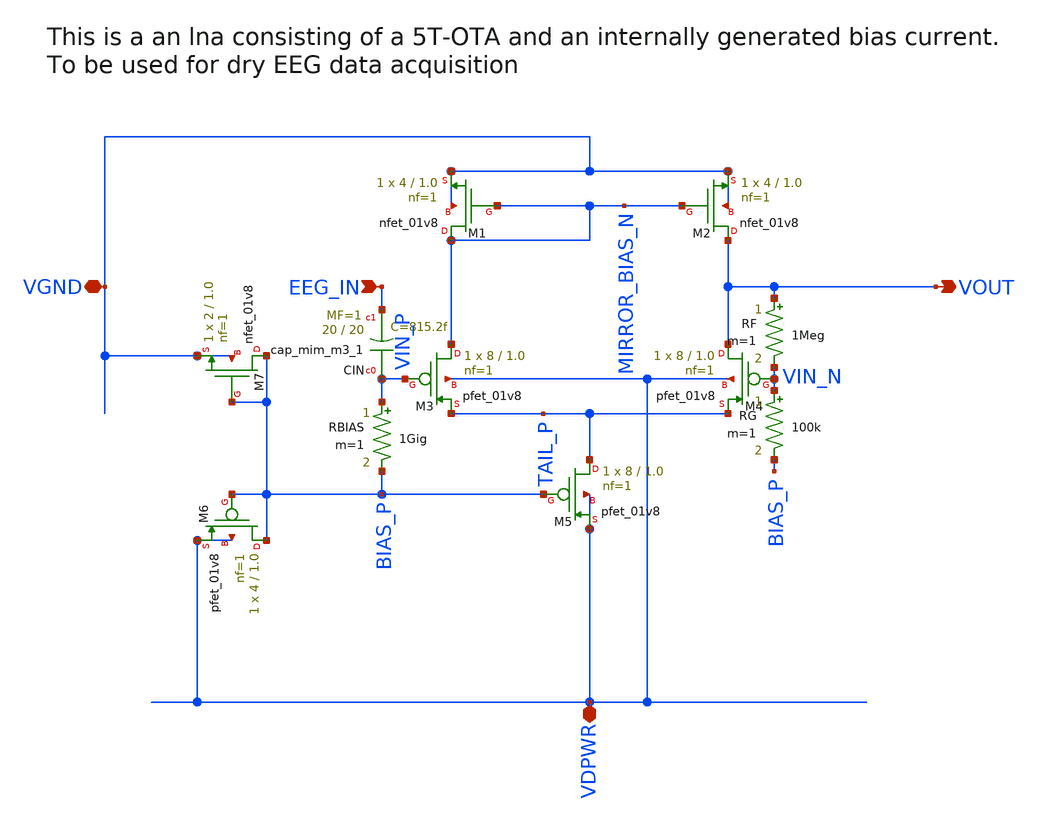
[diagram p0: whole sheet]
** sch_path: xschem/eeg_lna.sch
**.subckt eeg_lna VGND EEG_IN VDPWR VOUT
*.iopin VGND
*.ipin EEG_IN
*.iopin VDPWR
*.opin VOUT
XM1 MIRROR_BIAS_N MIRROR_BIAS_N VGND VGND sky130_fd_pr__nfet_01v8 L=1.0 W=4 nf=1 ad='int((1 + 1)/2) * 4 / 1 * 0.29'
+ as='int((1 + 2)/2) * 4 / 1 * 0.29' pd='2*int((1 + 1)/2) * (4 / 1 + 0.29)' ps='2*int((1 + 2)/2) * (4 / 1 + 0.29)'
+ nrd='0.29 / 4 ' nrs='0.29 / 4 ' sa=0 sb=0 sd=0 mult=1 m=1
XM2 VOUT MIRROR_BIAS_N VGND VGND sky130_fd_pr__nfet_01v8 L=1.0 W=4 nf=1 ad='int((1 + 1)/2) * 4 / 1 * 0.29'
+ as='int((1 + 2)/2) * 4 / 1 * 0.29' pd='2*int((1 + 1)/2) * (4 / 1 + 0.29)' ps='2*int((1 + 2)/2) * (4 / 1 + 0.29)'
+ nrd='0.29 / 4 ' nrs='0.29 / 4 ' sa=0 sb=0 sd=0 mult=1 m=1
XM3 MIRROR_BIAS_N VIN_P TAIL_P VDPWR sky130_fd_pr__pfet_01v8 L=1.0 W=8 nf=1 ad='int((1 + 1)/2) * 8 / 1 * 0.29'
+ as='int((1 + 2)/2) * 8 / 1 * 0.29' pd='2*int((1 + 1)/2) * (8 / 1 + 0.29)' ps='2*int((1 + 2)/2) * (8 / 1 + 0.29)'
+ nrd='0.29 / 8 ' nrs='0.29 / 8 ' sa=0 sb=0 sd=0 mult=1 m=1
XM4 VOUT VIN_N TAIL_P VDPWR sky130_fd_pr__pfet_01v8 L=1.0 W=8 nf=1 ad='int((1 + 1)/2) * 8 / 1 * 0.29'
+ as='int((1 + 2)/2) * 8 / 1 * 0.29' pd='2*int((1 + 1)/2) * (8 / 1 + 0.29)' ps='2*int((1 + 2)/2) * (8 / 1 + 0.29)'
+ nrd='0.29 / 8 ' nrs='0.29 / 8 ' sa=0 sb=0 sd=0 mult=1 m=1
XM5 TAIL_P BIAS_P VDPWR VDPWR sky130_fd_pr__pfet_01v8 L=1.0 W=8 nf=1 ad='int((1 + 1)/2) * 8 / 1 * 0.29'
+ as='int((1 + 2)/2) * 8 / 1 * 0.29' pd='2*int((1 + 1)/2) * (8 / 1 + 0.29)' ps='2*int((1 + 2)/2) * (8 / 1 + 0.29)'
+ nrd='0.29 / 8 ' nrs='0.29 / 8 ' sa=0 sb=0 sd=0 mult=1 m=1
XM6 BIAS_P BIAS_P VDPWR VDPWR sky130_fd_pr__pfet_01v8 L=1.0 W=4 nf=1 ad='int((1 + 1)/2) * 4 / 1 * 0.29'
+ as='int((1 + 2)/2) * 4 / 1 * 0.29' pd='2*int((1 + 1)/2) * (4 / 1 + 0.29)' ps='2*int((1 + 2)/2) * (4 / 1 + 0.29)'
+ nrd='0.29 / 4 ' nrs='0.29 / 4 ' sa=0 sb=0 sd=0 mult=1 m=1
XM7 BIAS_P BIAS_P VGND VGND sky130_fd_pr__nfet_01v8 L=1.0 W=2 nf=1 ad='int((1 + 1)/2) * 2 / 1 * 0.29'
+ as='int((1 + 2)/2) * 2 / 1 * 0.29' pd='2*int((1 + 1)/2) * (2 / 1 + 0.29)' ps='2*int((1 + 2)/2) * (2 / 1 + 0.29)'
+ nrd='0.29 / 2 ' nrs='0.29 / 2 ' sa=0 sb=0 sd=0 mult=1 m=1
XCIN VIN_P EEG_IN sky130_fd_pr__cap_mim_m3_1 W=20 L=20 MF=1 m=1
RBIAS VIN_P BIAS_P 1Gig m=1
RF VOUT VIN_N 1Meg m=1
RG VIN_N BIAS_P 100k m=1
**.ends
.end
